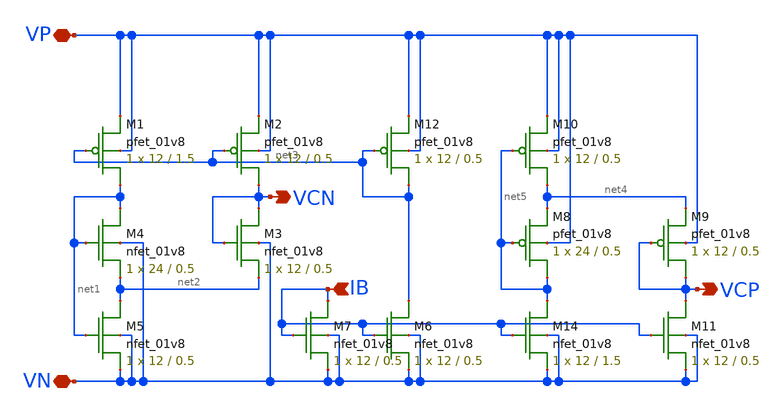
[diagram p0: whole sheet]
** sch_path: mp3/schematics/bias_generator (copy).sch
**.subckt bias_generator (copy) VCN VP VN IB VCP
*.opin VCN
*.iopin VP
*.iopin VN
*.ipin IB
*.opin VCP
XM1 net1 net3 VP VP sky130_fd_pr__pfet_01v8 L=1.5 W=12 nf=1 ad='int((nf+1)/2) * W/nf * 0.29' as='int((nf+2)/2) * W/nf * 0.29'
+ pd='2*int((nf+1)/2) * (W/nf + 0.29)' ps='2*int((nf+2)/2) * (W/nf + 0.29)' nrd='0.29 / W' nrs='0.29 / W'
+ sa=0 sb=0 sd=0 mult=1 m=1
XM2 VCN net3 VP VP sky130_fd_pr__pfet_01v8 L=0.5 W=12 nf=1 ad='int((nf+1)/2) * W/nf * 0.29' as='int((nf+2)/2) * W/nf * 0.29'
+ pd='2*int((nf+1)/2) * (W/nf + 0.29)' ps='2*int((nf+2)/2) * (W/nf + 0.29)' nrd='0.29 / W' nrs='0.29 / W'
+ sa=0 sb=0 sd=0 mult=1 m=1
XM8 net5 net5 net4 VP sky130_fd_pr__pfet_01v8 L=0.5 W=24 nf=1 ad='int((nf+1)/2) * W/nf * 0.29' as='int((nf+2)/2) * W/nf * 0.29'
+ pd='2*int((nf+1)/2) * (W/nf + 0.29)' ps='2*int((nf+2)/2) * (W/nf + 0.29)' nrd='0.29 / W' nrs='0.29 / W'
+ sa=0 sb=0 sd=0 mult=1 m=1
XM9 VCP VCP net4 VP sky130_fd_pr__pfet_01v8 L=0.5 W=12 nf=1 ad='int((nf+1)/2) * W/nf * 0.29' as='int((nf+2)/2) * W/nf * 0.29'
+ pd='2*int((nf+1)/2) * (W/nf + 0.29)' ps='2*int((nf+2)/2) * (W/nf + 0.29)' nrd='0.29 / W' nrs='0.29 / W'
+ sa=0 sb=0 sd=0 mult=1 m=1
XM10 net4 net5 VP VP sky130_fd_pr__pfet_01v8 L=0.5 W=12 nf=1 ad='int((nf+1)/2) * W/nf * 0.29' as='int((nf+2)/2) * W/nf * 0.29'
+ pd='2*int((nf+1)/2) * (W/nf + 0.29)' ps='2*int((nf+2)/2) * (W/nf + 0.29)' nrd='0.29 / W' nrs='0.29 / W'
+ sa=0 sb=0 sd=0 mult=1 m=1
XM11 VCP IB VN VN sky130_fd_pr__nfet_01v8 L=0.5 W=12 nf=1 ad='int((nf+1)/2) * W/nf * 0.29' as='int((nf+2)/2) * W/nf * 0.29'
+ pd='2*int((nf+1)/2) * (W/nf + 0.29)' ps='2*int((nf+2)/2) * (W/nf + 0.29)' nrd='0.29 / W' nrs='0.29 / W'
+ sa=0 sb=0 sd=0 mult=1 m=1
XM14 net5 IB VN VN sky130_fd_pr__nfet_01v8 L=1.5 W=12 nf=1 ad='int((nf+1)/2) * W/nf * 0.29' as='int((nf+2)/2) * W/nf * 0.29'
+ pd='2*int((nf+1)/2) * (W/nf + 0.29)' ps='2*int((nf+2)/2) * (W/nf + 0.29)' nrd='0.29 / W' nrs='0.29 / W'
+ sa=0 sb=0 sd=0 mult=1 m=1
XM6 net3 IB VN VN sky130_fd_pr__nfet_01v8 L=0.5 W=12 nf=1 ad='int((nf+1)/2) * W/nf * 0.29' as='int((nf+2)/2) * W/nf * 0.29'
+ pd='2*int((nf+1)/2) * (W/nf + 0.29)' ps='2*int((nf+2)/2) * (W/nf + 0.29)' nrd='0.29 / W' nrs='0.29 / W'
+ sa=0 sb=0 sd=0 mult=1 m=1
XM7 IB IB VN VN sky130_fd_pr__nfet_01v8 L=0.5 W=12 nf=1 ad='int((nf+1)/2) * W/nf * 0.29' as='int((nf+2)/2) * W/nf * 0.29'
+ pd='2*int((nf+1)/2) * (W/nf + 0.29)' ps='2*int((nf+2)/2) * (W/nf + 0.29)' nrd='0.29 / W' nrs='0.29 / W'
+ sa=0 sb=0 sd=0 mult=1 m=1
XM3 VCN VCN net2 VN sky130_fd_pr__nfet_01v8 L=0.5 W=12 nf=1 ad='int((nf+1)/2) * W/nf * 0.29' as='int((nf+2)/2) * W/nf * 0.29'
+ pd='2*int((nf+1)/2) * (W/nf + 0.29)' ps='2*int((nf+2)/2) * (W/nf + 0.29)' nrd='0.29 / W' nrs='0.29 / W'
+ sa=0 sb=0 sd=0 mult=1 m=1
XM4 net1 net1 net2 VN sky130_fd_pr__nfet_01v8 L=0.5 W=24 nf=1 ad='int((nf+1)/2) * W/nf * 0.29' as='int((nf+2)/2) * W/nf * 0.29'
+ pd='2*int((nf+1)/2) * (W/nf + 0.29)' ps='2*int((nf+2)/2) * (W/nf + 0.29)' nrd='0.29 / W' nrs='0.29 / W'
+ sa=0 sb=0 sd=0 mult=1 m=1
XM5 net2 net1 VN VN sky130_fd_pr__nfet_01v8 L=0.5 W=12 nf=1 ad='int((nf+1)/2) * W/nf * 0.29' as='int((nf+2)/2) * W/nf * 0.29'
+ pd='2*int((nf+1)/2) * (W/nf + 0.29)' ps='2*int((nf+2)/2) * (W/nf + 0.29)' nrd='0.29 / W' nrs='0.29 / W'
+ sa=0 sb=0 sd=0 mult=1 m=1
XM12 net3 net3 VP VP sky130_fd_pr__pfet_01v8 L=0.5 W=12 nf=1 ad='int((nf+1)/2) * W/nf * 0.29' as='int((nf+2)/2) * W/nf * 0.29'
+ pd='2*int((nf+1)/2) * (W/nf + 0.29)' ps='2*int((nf+2)/2) * (W/nf + 0.29)' nrd='0.29 / W' nrs='0.29 / W'
+ sa=0 sb=0 sd=0 mult=1 m=1
**.ends
.end
